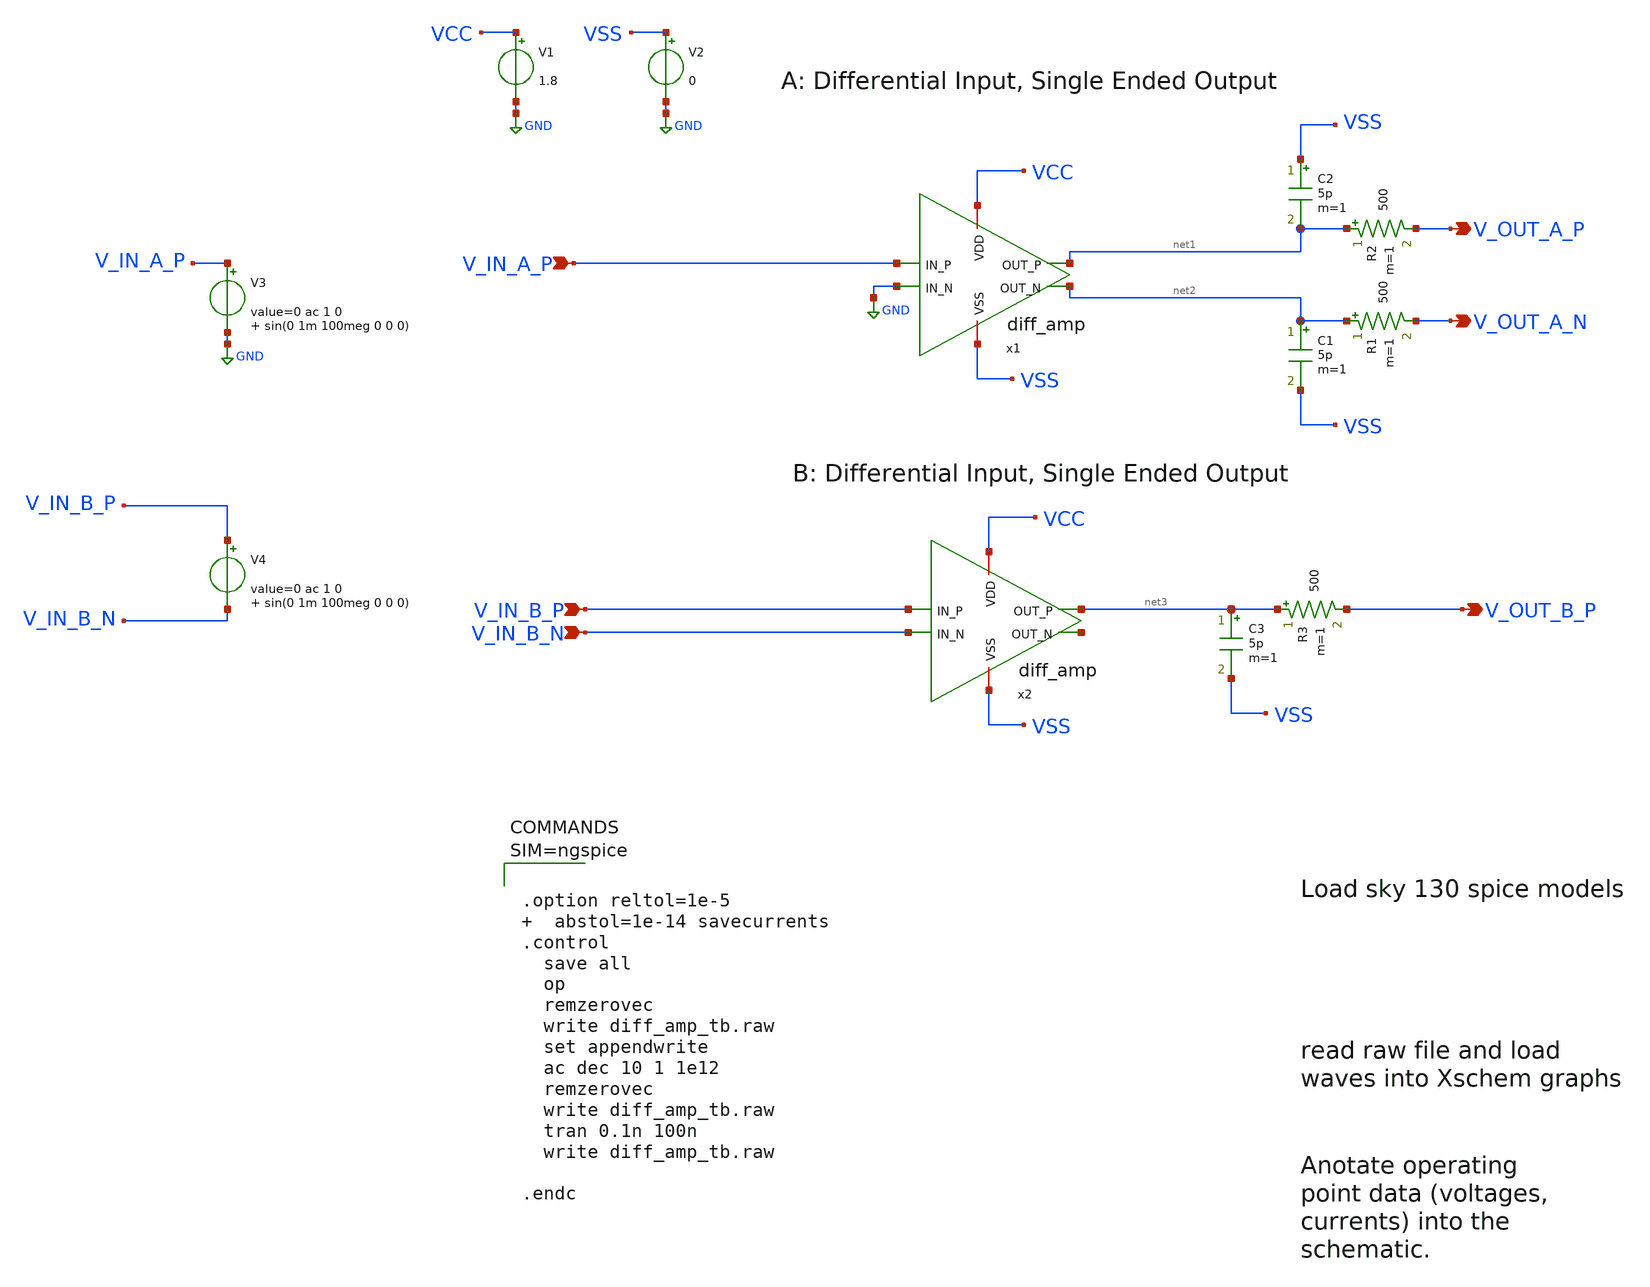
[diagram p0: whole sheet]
** sch_path: xschem/diff_amp_tb.sch
**.subckt diff_amp_tb V_IN_A_P V_OUT_A_N V_IN_B_P V_OUT_B_P V_IN_B_N V_OUT_A_P
*.ipin V_IN_A_P
*.opin V_OUT_A_N
*.ipin V_IN_B_P
*.opin V_OUT_B_P
*.ipin V_IN_B_N
*.opin V_OUT_A_P
x1 VCC VSS GND net1 net2 V_IN_A_P diff_amp
V1 VCC GND 1.8
V2 VSS GND 0
x2 VCC VSS V_IN_B_N net3 net4 V_IN_B_P diff_amp
R1 net2 V_OUT_A_N 500 m=1
C1 net2 VSS 5p m=1
R2 net1 V_OUT_A_P 500 m=1
C2 VSS net1 5p m=1
C3 net3 VSS 5p m=1
R3 net3 V_OUT_B_P 500 m=1
V3 V_IN_A_P GND 0 ac 1 0 sin(0 1m 100meg 0 0 0)
V4 V_IN_B_P V_IN_B_N 0 ac 1 0 sin(0 1m 100meg 0 0 0)
**** begin user architecture code

** opencircuitdesign pdks install
.lib $::SKYWATER_MODELS/sky130.lib.spice tt





.option reltol=1e-5   abstol=1e-14 savecurrents
.control
  save all
  op
  remzerovec
  write diff_amp_tb.raw
  set appendwrite
  ac dec 10 1 1e12
  remzerovec
  write diff_amp_tb.raw
  tran 0.1n 100n
  write diff_amp_tb.raw

.endc



**** end user architecture code
**.ends

* expanding   symbol:  diff_amp.sym # of pins=6
** sym_path: xschem/diff_amp.sym
** sch_path: xschem/diff_amp.sch
.subckt diff_amp VDD VSS IN_N OUT_P OUT_N IN_P
*.iopin VDD
*.iopin VSS
*.ipin IN_N
*.ipin IN_P
*.opin OUT_P
*.opin OUT_N
XM3 VX net1 VSS VSS sky130_fd_pr__nfet_01v8 L=2 W=4 nf=4 ad='int((nf+1)/2) * W/nf * 0.29' as='int((nf+2)/2) * W/nf * 0.29'
+ pd='2*int((nf+1)/2) * (W/nf + 0.29)' ps='2*int((nf+2)/2) * (W/nf + 0.29)' nrd='0.29 / W' nrs='0.29 / W'
+ sa=0 sb=0 sd=0 mult=1 m=1
XM6 net1 net1 VSS VSS sky130_fd_pr__nfet_01v8 L=2 W=4 nf=4 ad='int((nf+1)/2) * W/nf * 0.29' as='int((nf+2)/2) * W/nf * 0.29'
+ pd='2*int((nf+1)/2) * (W/nf + 0.29)' ps='2*int((nf+2)/2) * (W/nf + 0.29)' nrd='0.29 / W' nrs='0.29 / W'
+ sa=0 sb=0 sd=0 mult=1 m=1
XR1 net1 VDD VSS sky130_fd_pr__res_xhigh_po_0p35 L=2.8 mult=1 m=1
XM2 OUT_P IN_P VX VSS sky130_fd_pr__nfet_01v8_lvt L=0.5 W=2.5 nf=1 ad='int((nf+1)/2) * W/nf * 0.29' as='int((nf+2)/2) * W/nf * 0.29'
+ pd='2*int((nf+1)/2) * (W/nf + 0.29)' ps='2*int((nf+2)/2) * (W/nf + 0.29)' nrd='0.29 / W' nrs='0.29 / W'
+ sa=0 sb=0 sd=0 mult=1 m=1
XM1 OUT_N IN_N VX VSS sky130_fd_pr__nfet_01v8_lvt L=0.5 W=2.5 nf=1 ad='int((nf+1)/2) * W/nf * 0.29' as='int((nf+2)/2) * W/nf * 0.29'
+ pd='2*int((nf+1)/2) * (W/nf + 0.29)' ps='2*int((nf+2)/2) * (W/nf + 0.29)' nrd='0.29 / W' nrs='0.29 / W'
+ sa=0 sb=0 sd=0 mult=1 m=1
XM4 OUT_P OUT_P VDD VDD sky130_fd_pr__pfet_01v8_lvt L=2 W=6 nf=6 ad='int((nf+1)/2) * W/nf * 0.29' as='int((nf+2)/2) * W/nf * 0.29'
+ pd='2*int((nf+1)/2) * (W/nf + 0.29)' ps='2*int((nf+2)/2) * (W/nf + 0.29)' nrd='0.29 / W' nrs='0.29 / W'
+ sa=0 sb=0 sd=0 mult=1 m=1
XM5 OUT_N OUT_P VDD VDD sky130_fd_pr__pfet_01v8_lvt L=2 W=6 nf=6 ad='int((nf+1)/2) * W/nf * 0.29' as='int((nf+2)/2) * W/nf * 0.29'
+ pd='2*int((nf+1)/2) * (W/nf + 0.29)' ps='2*int((nf+2)/2) * (W/nf + 0.29)' nrd='0.29 / W' nrs='0.29 / W'
+ sa=0 sb=0 sd=0 mult=1 m=1
.ends

.GLOBAL GND
.end
